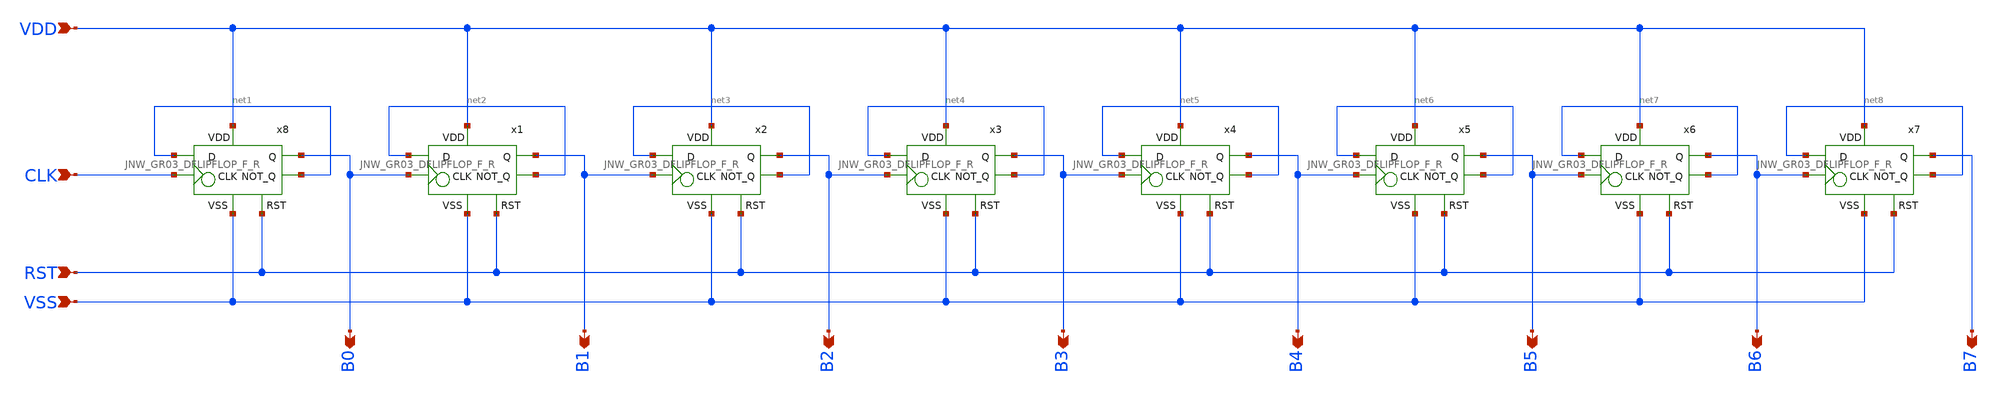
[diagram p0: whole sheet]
** sch_path: design/JNW_GR03_SKY130A/JNW_GR03_8BCOUNTER.sch
**.subckt JNW_GR03_8BCOUNTER VDD VSS CLK B0 B1 B2 B3 B4 B5 B6 B7 RST
*.ipin VDD
*.ipin VSS
*.ipin CLK
*.opin B0
*.opin B1
*.opin B2
*.opin B3
*.opin B4
*.opin B5
*.opin B6
*.opin B7
*.ipin RST
x7 VDD B7 net8 B6 net8 RST VSS JNW_GR03_DFLIPFLOP_F_R
x6 VDD B6 net7 B5 net7 RST VSS JNW_GR03_DFLIPFLOP_F_R
x5 VDD B5 net6 B4 net6 RST VSS JNW_GR03_DFLIPFLOP_F_R
x4 VDD B4 net5 B3 net5 RST VSS JNW_GR03_DFLIPFLOP_F_R
x3 VDD B3 net4 B2 net4 RST VSS JNW_GR03_DFLIPFLOP_F_R
x2 VDD B2 net3 B1 net3 RST VSS JNW_GR03_DFLIPFLOP_F_R
x1 VDD B1 net2 B0 net2 RST VSS JNW_GR03_DFLIPFLOP_F_R
x8 VDD B0 net1 CLK net1 RST VSS JNW_GR03_DFLIPFLOP_F_R
**.ends
.end
